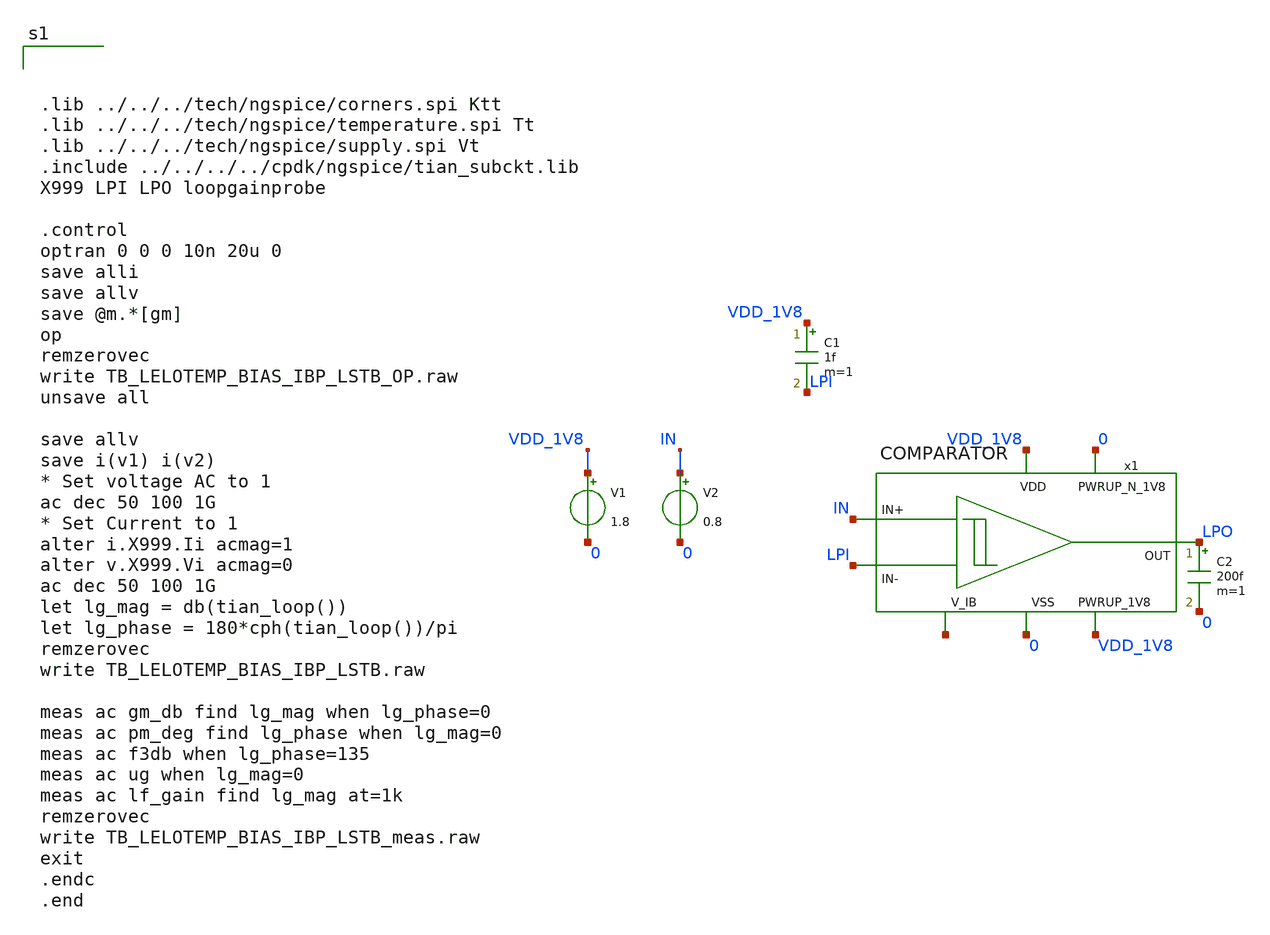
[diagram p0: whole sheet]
** sch_path: design/LELO_GR03_SKY130A/BP_OTA.sch
**.subckt BP_OTA
V1 VDD_1V8 0 1.8
C1 VDD_1V8 LPI 1f m=1
V2 IN 0 0.8
C2 LPO 0 200f m=1
x1 VDD_1V8 IN LPO LPI 0 0 VDD_1V8 net1 COMPARATOR
**** begin user architecture code



.lib ../../../tech/ngspice/corners.spi Ktt
.lib ../../../tech/ngspice/temperature.spi Tt
.lib ../../../tech/ngspice/supply.spi Vt
.include ../../../../cpdk/ngspice/tian_subckt.lib
X999 LPI LPO loopgainprobe

.control
optran 0 0 0 10n 20u 0
save alli
save allv
save @m.*[gm]
op
remzerovec
write TB_LELOTEMP_BIAS_IBP_LSTB_OP.raw
unsave all

save allv
save i(v1) i(v2)
* Set voltage AC to 1
ac dec 50 100 1G
* Set Current to 1
alter i.X999.Ii acmag=1
alter v.X999.Vi acmag=0
ac dec 50 100 1G
let lg_mag = db(tian_loop())
let lg_phase = 180*cph(tian_loop())/pi
remzerovec
write TB_LELOTEMP_BIAS_IBP_LSTB.raw

meas ac gm_db find lg_mag when lg_phase=0
meas ac pm_deg find lg_phase when lg_mag=0
meas ac f3db when lg_phase=135
meas ac ug when lg_mag=0
meas ac lf_gain find lg_mag at=1k
remzerovec
write TB_LELOTEMP_BIAS_IBP_LSTB_meas.raw
exit
.endc
.end



**** end user architecture code
**.ends
.end
